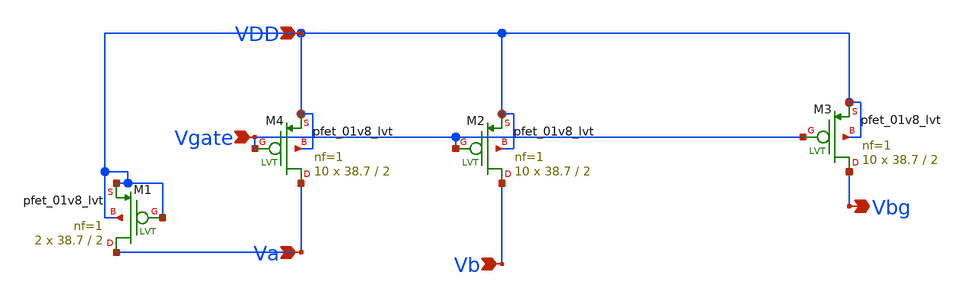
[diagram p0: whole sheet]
** sch_path: lvs/currentMirrorGold.sch
**.subckt currentMirrorGold Vgate Va Vb Vbg VDD
*.ipin Vgate
*.ipin Va
*.ipin Vb
*.opin Vbg
*.ipin VDD
XM2 Vb Vgate VDD VDD sky130_fd_pr__pfet_01v8_lvt L=2 W=38.7 nf=1 ad='int((nf+1)/2) * W/nf * 0.29' as='int((nf+2)/2) * W/nf * 0.29'
+ pd='2*int((nf+1)/2) * (W/nf + 0.29)' ps='2*int((nf+2)/2) * (W/nf + 0.29)' nrd='0.29 / W' nrs='0.29 / W'
+ sa=0 sb=0 sd=0 mult=10 m=10
XM3 Vbg Vgate VDD VDD sky130_fd_pr__pfet_01v8_lvt L=2 W=38.7 nf=1 ad='int((nf+1)/2) * W/nf * 0.29' as='int((nf+2)/2) * W/nf * 0.29'
+ pd='2*int((nf+1)/2) * (W/nf + 0.29)' ps='2*int((nf+2)/2) * (W/nf + 0.29)' nrd='0.29 / W' nrs='0.29 / W'
+ sa=0 sb=0 sd=0 mult=10 m=10
XM4 Va Vgate VDD VDD sky130_fd_pr__pfet_01v8_lvt L=2 W=38.7 nf=1 ad='int((nf+1)/2) * W/nf * 0.29' as='int((nf+2)/2) * W/nf * 0.29'
+ pd='2*int((nf+1)/2) * (W/nf + 0.29)' ps='2*int((nf+2)/2) * (W/nf + 0.29)' nrd='0.29 / W' nrs='0.29 / W'
+ sa=0 sb=0 sd=0 mult=10 m=10
XM1 Va VDD VDD VDD sky130_fd_pr__pfet_01v8_lvt L=2 W=38.7 nf=1 ad='int((nf+1)/2) * W/nf * 0.29' as='int((nf+2)/2) * W/nf * 0.29'
+ pd='2*int((nf+1)/2) * (W/nf + 0.29)' ps='2*int((nf+2)/2) * (W/nf + 0.29)' nrd='0.29 / W' nrs='0.29 / W'
+ sa=0 sb=0 sd=0 mult=2 m=2
**.ends
.end
